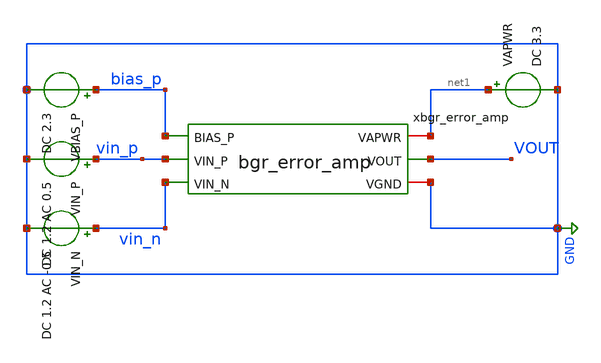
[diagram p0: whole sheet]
** sch_path: xschem/tb_bgr_error_amp.sch
**.subckt tb_bgr_error_amp
VBIAS_P bias_p GND DC 2.3
VIN_P vin_p GND DC 1.2 AC 0.5
VIN_N vin_n GND DC 1.2 AC -0.5
VAPWR net1 GND DC 3.3
xbgr_error_amp bias_p net1 vin_p vin_n VOUT GND bgr_error_amp
**** begin user architecture code


.param sw_stat_global=1  ; enable statistical variation (0 = OFF, 1 = ON)
.param mc_skew=1         ; MOS variation scale factor (1 = Nominal)
.param res_mc_skew=1     ; resistor variation scale factor (1 = Nominal)
.param fnoicor=0         ; flicker noise model selector
.param sw_stat_mismatch=0
.lib /foss/pdks/gf180mcuD/libs.tech/ngspice/sm141064.ngspice statistical
.control
op
ac dec 100 1 1e9
plot db(v(VOUT))
.endc


**** end user architecture code
**.ends

* expanding   symbol:  bgr_error_amp.sym # of pins=6
** sym_path: xschem/bgr_error_amp.sym
** sch_path: xschem/bgr_error_amp.sch
.subckt bgr_error_amp BIAS_P VAPWR VIN_P VIN_N VOUT VGND
*.ipin VIN_P
*.ipin VIN_N
*.ipin BIAS_P
*.iopin VAPWR
*.iopin VGND
*.opin VOUT
XMDIFF_P net1 VIN_P TAIL_P VAPWR pfet_03v3 L=0.28u W=0.22u nf=1 ad='int((nf+1)/2) * W/nf * 0.18u' as='int((nf+2)/2) * W/nf * 0.18u'
+ pd='2*int((nf+1)/2) * (W/nf + 0.18u)' ps='2*int((nf+2)/2) * (W/nf + 0.18u)' nrd='0.18u / W' nrs='0.18u / W'
+ sa=0 sb=0 sd=0 m=1
XMDIFF_N VOUT VIN_N TAIL_P VAPWR pfet_03v3 L=0.28u W=0.22u nf=1 ad='int((nf+1)/2) * W/nf * 0.18u' as='int((nf+2)/2) * W/nf * 0.18u'
+ pd='2*int((nf+1)/2) * (W/nf + 0.18u)' ps='2*int((nf+2)/2) * (W/nf + 0.18u)' nrd='0.18u / W' nrs='0.18u / W'
+ sa=0 sb=0 sd=0 m=1
XMTAIL TAIL_P BIAS_P VAPWR VAPWR pfet_03v3 L=0.28u W=0.22u nf=1 ad='int((nf+1)/2) * W/nf * 0.18u' as='int((nf+2)/2) * W/nf * 0.18u'
+ pd='2*int((nf+1)/2) * (W/nf + 0.18u)' ps='2*int((nf+2)/2) * (W/nf + 0.18u)' nrd='0.18u / W' nrs='0.18u / W'
+ sa=0 sb=0 sd=0 m=1
XMLOAD_REF net1 net1 VGND VGND nfet_03v3 L=0.28u W=0.22u nf=1 ad='int((nf+1)/2) * W/nf * 0.18u' as='int((nf+2)/2) * W/nf * 0.18u'
+ pd='2*int((nf+1)/2) * (W/nf + 0.18u)' ps='2*int((nf+2)/2) * (W/nf + 0.18u)' nrd='0.18u / W' nrs='0.18u / W'
+ sa=0 sb=0 sd=0 m=1
XMLOAD_OUT VOUT net1 VGND VGND nfet_03v3 L=0.28u W=0.22u nf=1 ad='int((nf+1)/2) * W/nf * 0.18u' as='int((nf+2)/2) * W/nf * 0.18u'
+ pd='2*int((nf+1)/2) * (W/nf + 0.18u)' ps='2*int((nf+2)/2) * (W/nf + 0.18u)' nrd='0.18u / W' nrs='0.18u / W'
+ sa=0 sb=0 sd=0 m=1
.ends

.GLOBAL GND
.end
